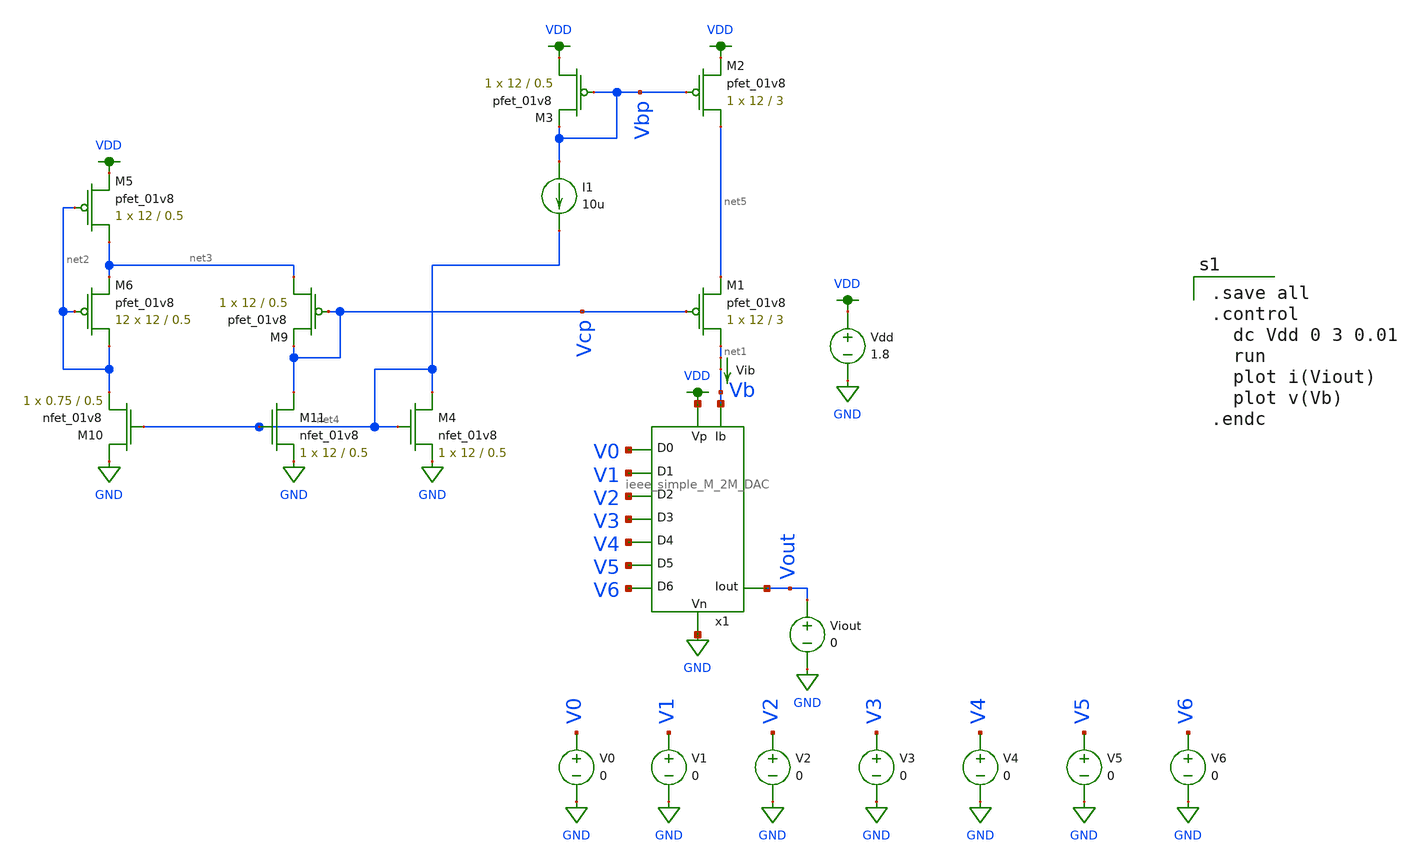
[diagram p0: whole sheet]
** sch_path: schematics/ieee DAC/characterization/top_voltage_sweep_with_cascode_and_vcn_generator.sch
**.subckt top_voltage_sweep_with_cascode_and_vcn_generator
Vdd VDD GND 1.8
V1 V1 GND 0
V2 V2 GND 0
V3 V3 GND 0
V4 V4 GND 0
V5 V5 GND 0
V6 V6 GND 0
V0 V0 GND 0
Viout Vout GND 0
Vib net1 Vb 0
.save i(vib)
x1 VDD Vout GND V1 V0 V2 V3 V4 V5 V6 Vb ieee_simple_M_2M_DAC
XM1 net1 Vcp net5 VDD sky130_fd_pr__pfet_01v8 L=3 W=12 nf=1 ad='int((nf+1)/2) * W/nf * 0.29' as='int((nf+2)/2) * W/nf * 0.29'
+ pd='2*int((nf+1)/2) * (W/nf + 0.29)' ps='2*int((nf+2)/2) * (W/nf + 0.29)' nrd='0.29 / W' nrs='0.29 / W'
+ sa=0 sb=0 sd=0 mult=1 m=1
XM5 net3 net2 VDD VDD sky130_fd_pr__pfet_01v8 L=0.5 W=12 nf=1 ad='int((nf+1)/2) * W/nf * 0.29' as='int((nf+2)/2) * W/nf * 0.29'
+ pd='2*int((nf+1)/2) * (W/nf + 0.29)' ps='2*int((nf+2)/2) * (W/nf + 0.29)' nrd='0.29 / W' nrs='0.29 / W'
+ sa=0 sb=0 sd=0 mult=1 m=1
XM6 net2 net2 net3 VDD sky130_fd_pr__pfet_01v8 L=0.5 W=12 nf=1 ad='int((nf+1)/2) * W/nf * 0.29' as='int((nf+2)/2) * W/nf * 0.29'
+ pd='2*int((nf+1)/2) * (W/nf + 0.29)' ps='2*int((nf+2)/2) * (W/nf + 0.29)' nrd='0.29 / W' nrs='0.29 / W'
+ sa=0 sb=0 sd=0 mult=12 m=12
XM9 net3 Vcp Vcp VDD sky130_fd_pr__pfet_01v8 L=0.5 W=12 nf=1 ad='int((nf+1)/2) * W/nf * 0.29' as='int((nf+2)/2) * W/nf * 0.29'
+ pd='2*int((nf+1)/2) * (W/nf + 0.29)' ps='2*int((nf+2)/2) * (W/nf + 0.29)' nrd='0.29 / W' nrs='0.29 / W'
+ sa=0 sb=0 sd=0 mult=1 m=1
XM10 GND net4 net2 GND sky130_fd_pr__nfet_01v8 L=0.5 W=0.75 nf=1 ad='int((nf+1)/2) * W/nf * 0.29' as='int((nf+2)/2) * W/nf * 0.29'
+ pd='2*int((nf+1)/2) * (W/nf + 0.29)' ps='2*int((nf+2)/2) * (W/nf + 0.29)' nrd='0.29 / W' nrs='0.29 / W'
+ sa=0 sb=0 sd=0 mult=1 m=1
XM11 Vcp net4 GND GND sky130_fd_pr__nfet_01v8 L=0.5 W=12 nf=1 ad='int((nf+1)/2) * W/nf * 0.29' as='int((nf+2)/2) * W/nf * 0.29'
+ pd='2*int((nf+1)/2) * (W/nf + 0.29)' ps='2*int((nf+2)/2) * (W/nf + 0.29)' nrd='0.29 / W' nrs='0.29 / W'
+ sa=0 sb=0 sd=0 mult=1 m=1
I1 Vbp net4 10u
XM2 net5 Vbp VDD VDD sky130_fd_pr__pfet_01v8 L=3 W=12 nf=1 ad='int((nf+1)/2) * W/nf * 0.29' as='int((nf+2)/2) * W/nf * 0.29'
+ pd='2*int((nf+1)/2) * (W/nf + 0.29)' ps='2*int((nf+2)/2) * (W/nf + 0.29)' nrd='0.29 / W' nrs='0.29 / W'
+ sa=0 sb=0 sd=0 mult=1 m=1
XM3 VDD Vbp Vbp VDD sky130_fd_pr__pfet_01v8 L=0.5 W=12 nf=1 ad='int((nf+1)/2) * W/nf * 0.29' as='int((nf+2)/2) * W/nf * 0.29'
+ pd='2*int((nf+1)/2) * (W/nf + 0.29)' ps='2*int((nf+2)/2) * (W/nf + 0.29)' nrd='0.29 / W' nrs='0.29 / W'
+ sa=0 sb=0 sd=0 mult=1 m=1
XM4 net4 net4 GND GND sky130_fd_pr__nfet_01v8 L=0.5 W=12 nf=1 ad='int((nf+1)/2) * W/nf * 0.29' as='int((nf+2)/2) * W/nf * 0.29'
+ pd='2*int((nf+1)/2) * (W/nf + 0.29)' ps='2*int((nf+2)/2) * (W/nf + 0.29)' nrd='0.29 / W' nrs='0.29 / W'
+ sa=0 sb=0 sd=0 mult=1 m=1
**** begin user architecture code

.option wnflag=1
.param MC_SWITCH=1.0
.lib ~/skywater/skywater-pdk/libraries/sky130_fd_pr_ngspice/latest/models/sky130.lib.spice tt


.save all
.control
  dc Vdd 0 3 0.01
  run
  plot i(Viout)
  plot v(Vb)
.endc

**** end user architecture code
**.ends

* expanding   symbol:  /home/madvlsi/dev/git/7-bit-D-A-converter-MP4-MADVLSI/schematics/ieee
*+ DAC/ieee_simple_M_2M_DAC.sym # of pins=11
** sym_path: mp4_submission/DAC/schematics/ieee_simple_M_2M_DAC.sym
** sch_path: mp4_submission/DAC/schematics/ieee_simple_M_2M_DAC.sch
.subckt ieee_simple_M_2M_DAC VDD Iout GND D1 D0 D2 D3 D4 D5 D6 Ibias
*.ipin Ibias
*.opin Iout
*.ipin D0
*.ipin D1
*.ipin D2
*.ipin D3
*.ipin D4
*.ipin D5
*.ipin D6
*.iopin VDD
*.iopin GND
x1 VDD GND net8 GND inverter
x2 VDD D0 net1 GND inverter
x3 VDD D1 net2 GND inverter
x4 VDD D2 net3 GND inverter
x5 VDD D3 net4 GND inverter
x6 VDD D4 net5 GND inverter
x7 VDD D5 net6 GND inverter
x8 VDD D6 net7 GND inverter
x9 Ibias net8 net1 net3 net4 net5 net6 D5 net2 D0 D1 D2 D3 D4 net7 D6 Iout GND ieee_DAC
.ends


* expanding   symbol:  /home/madvlsi/dev/git/7-bit-D-A-converter-MP4-MADVLSI/schematics/ieee
*+ DAC/inverter.sym # of pins=4
** sym_path: schematics/ieee DAC/inverter.sym
** sch_path: schematics/ieee DAC/inverter.sch
.subckt inverter VDD A Y GND
*.ipin A
*.iopin VDD
*.iopin GND
*.opin Y
XM1 Y A GND GND sky130_fd_pr__nfet_01v8 L=0.5 W=12 nf=1 ad='int((nf+1)/2) * W/nf * 0.29' as='int((nf+2)/2) * W/nf * 0.29'
+ pd='2*int((nf+1)/2) * (W/nf + 0.29)' ps='2*int((nf+2)/2) * (W/nf + 0.29)' nrd='0.29 / W' nrs='0.29 / W'
+ sa=0 sb=0 sd=0 mult=1 m=1
XM2 Y A VDD VDD sky130_fd_pr__pfet_01v8 L=0.5 W=12 nf=1 ad='int((nf+1)/2) * W/nf * 0.29' as='int((nf+2)/2) * W/nf * 0.29'
+ pd='2*int((nf+1)/2) * (W/nf + 0.29)' ps='2*int((nf+2)/2) * (W/nf + 0.29)' nrd='0.29 / W' nrs='0.29 / W'
+ sa=0 sb=0 sd=0 mult=1 m=1
.ends


* expanding   symbol:  /home/madvlsi/dev/git/7-bit-D-A-converter-MP4-MADVLSI/schematics/ieee
*+ DAC/ieee_DAC.sym # of pins=18
** sym_path: schematics/ieee DAC/ieee_DAC.sym
** sch_path: schematics/ieee DAC/ieee_DAC.sch
.subckt ieee_DAC Ibias Vg D0 D2 D3 D4 D5 D5b D1 D0b D1b D2b D3b D4b D6 D6b Iout Idump
*.ipin D0
*.ipin D1
*.ipin D2
*.ipin D3
*.ipin D4
*.ipin D5
*.ipin D6
*.ipin D0b
*.ipin D1b
*.ipin D2b
*.ipin D3b
*.ipin D4b
*.ipin D5b
*.ipin D6b
*.iopin Iout
*.iopin Idump
*.iopin Ibias
*.iopin Vg
XM1 Ibias Vg net12 GND sky130_fd_pr__nfet_01v8 L=0.5 W=12 nf=1 ad='int((nf+1)/2) * W/nf * 0.29' as='int((nf+2)/2) * W/nf * 0.29'
+ pd='2*int((nf+1)/2) * (W/nf + 0.29)' ps='2*int((nf+2)/2) * (W/nf + 0.29)' nrd='0.29 / W' nrs='0.29 / W'
+ sa=0 sb=0 sd=0 mult=1 m=1
XM4 Ibias Vg net1 GND sky130_fd_pr__nfet_01v8 L=0.5 W=12 nf=1 ad='int((nf+1)/2) * W/nf * 0.29' as='int((nf+2)/2) * W/nf * 0.29'
+ pd='2*int((nf+1)/2) * (W/nf + 0.29)' ps='2*int((nf+2)/2) * (W/nf + 0.29)' nrd='0.29 / W' nrs='0.29 / W'
+ sa=0 sb=0 sd=0 mult=1 m=1
XM5 net1 Vg net11 GND sky130_fd_pr__nfet_01v8 L=0.5 W=12 nf=1 ad='int((nf+1)/2) * W/nf * 0.29' as='int((nf+2)/2) * W/nf * 0.29'
+ pd='2*int((nf+1)/2) * (W/nf + 0.29)' ps='2*int((nf+2)/2) * (W/nf + 0.29)' nrd='0.29 / W' nrs='0.29 / W'
+ sa=0 sb=0 sd=0 mult=1 m=1
XM8 net1 Vg net2 GND sky130_fd_pr__nfet_01v8 L=0.5 W=12 nf=1 ad='int((nf+1)/2) * W/nf * 0.29' as='int((nf+2)/2) * W/nf * 0.29'
+ pd='2*int((nf+1)/2) * (W/nf + 0.29)' ps='2*int((nf+2)/2) * (W/nf + 0.29)' nrd='0.29 / W' nrs='0.29 / W'
+ sa=0 sb=0 sd=0 mult=1 m=1
XM9 net2 Vg net10 GND sky130_fd_pr__nfet_01v8 L=0.5 W=12 nf=1 ad='int((nf+1)/2) * W/nf * 0.29' as='int((nf+2)/2) * W/nf * 0.29'
+ pd='2*int((nf+1)/2) * (W/nf + 0.29)' ps='2*int((nf+2)/2) * (W/nf + 0.29)' nrd='0.29 / W' nrs='0.29 / W'
+ sa=0 sb=0 sd=0 mult=1 m=1
XM12 net2 Vg net3 GND sky130_fd_pr__nfet_01v8 L=0.5 W=12 nf=1 ad='int((nf+1)/2) * W/nf * 0.29' as='int((nf+2)/2) * W/nf * 0.29'
+ pd='2*int((nf+1)/2) * (W/nf + 0.29)' ps='2*int((nf+2)/2) * (W/nf + 0.29)' nrd='0.29 / W' nrs='0.29 / W'
+ sa=0 sb=0 sd=0 mult=1 m=1
XM13 net3 Vg net9 GND sky130_fd_pr__nfet_01v8 L=0.5 W=12 nf=1 ad='int((nf+1)/2) * W/nf * 0.29' as='int((nf+2)/2) * W/nf * 0.29'
+ pd='2*int((nf+1)/2) * (W/nf + 0.29)' ps='2*int((nf+2)/2) * (W/nf + 0.29)' nrd='0.29 / W' nrs='0.29 / W'
+ sa=0 sb=0 sd=0 mult=1 m=1
XM16 net3 Vg net4 GND sky130_fd_pr__nfet_01v8 L=0.5 W=12 nf=1 ad='int((nf+1)/2) * W/nf * 0.29' as='int((nf+2)/2) * W/nf * 0.29'
+ pd='2*int((nf+1)/2) * (W/nf + 0.29)' ps='2*int((nf+2)/2) * (W/nf + 0.29)' nrd='0.29 / W' nrs='0.29 / W'
+ sa=0 sb=0 sd=0 mult=1 m=1
XM17 net4 Vg net8 GND sky130_fd_pr__nfet_01v8 L=0.5 W=12 nf=1 ad='int((nf+1)/2) * W/nf * 0.29' as='int((nf+2)/2) * W/nf * 0.29'
+ pd='2*int((nf+1)/2) * (W/nf + 0.29)' ps='2*int((nf+2)/2) * (W/nf + 0.29)' nrd='0.29 / W' nrs='0.29 / W'
+ sa=0 sb=0 sd=0 mult=1 m=1
XM7 net4 Vg net5 GND sky130_fd_pr__nfet_01v8 L=0.5 W=12 nf=1 ad='int((nf+1)/2) * W/nf * 0.29' as='int((nf+2)/2) * W/nf * 0.29'
+ pd='2*int((nf+1)/2) * (W/nf + 0.29)' ps='2*int((nf+2)/2) * (W/nf + 0.29)' nrd='0.29 / W' nrs='0.29 / W'
+ sa=0 sb=0 sd=0 mult=1 m=1
XM10 net5 Vg net7 GND sky130_fd_pr__nfet_01v8 L=0.5 W=12 nf=1 ad='int((nf+1)/2) * W/nf * 0.29' as='int((nf+2)/2) * W/nf * 0.29'
+ pd='2*int((nf+1)/2) * (W/nf + 0.29)' ps='2*int((nf+2)/2) * (W/nf + 0.29)' nrd='0.29 / W' nrs='0.29 / W'
+ sa=0 sb=0 sd=0 mult=1 m=1
XM15 net5 Vg net6 GND sky130_fd_pr__nfet_01v8 L=0.5 W=12 nf=1 ad='int((nf+1)/2) * W/nf * 0.29' as='int((nf+2)/2) * W/nf * 0.29'
+ pd='2*int((nf+1)/2) * (W/nf + 0.29)' ps='2*int((nf+2)/2) * (W/nf + 0.29)' nrd='0.29 / W' nrs='0.29 / W'
+ sa=0 sb=0 sd=0 mult=1 m=1
XM18 net6 Vg net13 GND sky130_fd_pr__nfet_01v8 L=0.5 W=12 nf=1 ad='int((nf+1)/2) * W/nf * 0.29' as='int((nf+2)/2) * W/nf * 0.29'
+ pd='2*int((nf+1)/2) * (W/nf + 0.29)' ps='2*int((nf+2)/2) * (W/nf + 0.29)' nrd='0.29 / W' nrs='0.29 / W'
+ sa=0 sb=0 sd=0 mult=1 m=1
XM2 net7 D5 Iout GND sky130_fd_pr__nfet_01v8 L=0.5 W=12 nf=1 ad='int((nf+1)/2) * W/nf * 0.29' as='int((nf+2)/2) * W/nf * 0.29'
+ pd='2*int((nf+1)/2) * (W/nf + 0.29)' ps='2*int((nf+2)/2) * (W/nf + 0.29)' nrd='0.29 / W' nrs='0.29 / W'
+ sa=0 sb=0 sd=0 mult=1 m=1
XM3 Idump D5b net7 GND sky130_fd_pr__nfet_01v8 L=0.5 W=12 nf=1 ad='int((nf+1)/2) * W/nf * 0.29' as='int((nf+2)/2) * W/nf * 0.29'
+ pd='2*int((nf+1)/2) * (W/nf + 0.29)' ps='2*int((nf+2)/2) * (W/nf + 0.29)' nrd='0.29 / W' nrs='0.29 / W'
+ sa=0 sb=0 sd=0 mult=1 m=1
XM6 net8 D4 Iout GND sky130_fd_pr__nfet_01v8 L=0.5 W=12 nf=1 ad='int((nf+1)/2) * W/nf * 0.29' as='int((nf+2)/2) * W/nf * 0.29'
+ pd='2*int((nf+1)/2) * (W/nf + 0.29)' ps='2*int((nf+2)/2) * (W/nf + 0.29)' nrd='0.29 / W' nrs='0.29 / W'
+ sa=0 sb=0 sd=0 mult=1 m=1
XM11 Idump D4b net8 GND sky130_fd_pr__nfet_01v8 L=0.5 W=12 nf=1 ad='int((nf+1)/2) * W/nf * 0.29' as='int((nf+2)/2) * W/nf * 0.29'
+ pd='2*int((nf+1)/2) * (W/nf + 0.29)' ps='2*int((nf+2)/2) * (W/nf + 0.29)' nrd='0.29 / W' nrs='0.29 / W'
+ sa=0 sb=0 sd=0 mult=1 m=1
XM14 net9 D3 Iout GND sky130_fd_pr__nfet_01v8 L=0.5 W=12 nf=1 ad='int((nf+1)/2) * W/nf * 0.29' as='int((nf+2)/2) * W/nf * 0.29'
+ pd='2*int((nf+1)/2) * (W/nf + 0.29)' ps='2*int((nf+2)/2) * (W/nf + 0.29)' nrd='0.29 / W' nrs='0.29 / W'
+ sa=0 sb=0 sd=0 mult=1 m=1
XM19 Idump D3b net9 GND sky130_fd_pr__nfet_01v8 L=0.5 W=12 nf=1 ad='int((nf+1)/2) * W/nf * 0.29' as='int((nf+2)/2) * W/nf * 0.29'
+ pd='2*int((nf+1)/2) * (W/nf + 0.29)' ps='2*int((nf+2)/2) * (W/nf + 0.29)' nrd='0.29 / W' nrs='0.29 / W'
+ sa=0 sb=0 sd=0 mult=1 m=1
XM20 net10 D2 Iout GND sky130_fd_pr__nfet_01v8 L=0.5 W=12 nf=1 ad='int((nf+1)/2) * W/nf * 0.29' as='int((nf+2)/2) * W/nf * 0.29'
+ pd='2*int((nf+1)/2) * (W/nf + 0.29)' ps='2*int((nf+2)/2) * (W/nf + 0.29)' nrd='0.29 / W' nrs='0.29 / W'
+ sa=0 sb=0 sd=0 mult=1 m=1
XM21 Idump D2b net10 GND sky130_fd_pr__nfet_01v8 L=0.5 W=12 nf=1 ad='int((nf+1)/2) * W/nf * 0.29' as='int((nf+2)/2) * W/nf * 0.29'
+ pd='2*int((nf+1)/2) * (W/nf + 0.29)' ps='2*int((nf+2)/2) * (W/nf + 0.29)' nrd='0.29 / W' nrs='0.29 / W'
+ sa=0 sb=0 sd=0 mult=1 m=1
XM22 net11 D1 Iout GND sky130_fd_pr__nfet_01v8 L=0.5 W=12 nf=1 ad='int((nf+1)/2) * W/nf * 0.29' as='int((nf+2)/2) * W/nf * 0.29'
+ pd='2*int((nf+1)/2) * (W/nf + 0.29)' ps='2*int((nf+2)/2) * (W/nf + 0.29)' nrd='0.29 / W' nrs='0.29 / W'
+ sa=0 sb=0 sd=0 mult=1 m=1
XM23 Idump D1b net11 GND sky130_fd_pr__nfet_01v8 L=0.5 W=12 nf=1 ad='int((nf+1)/2) * W/nf * 0.29' as='int((nf+2)/2) * W/nf * 0.29'
+ pd='2*int((nf+1)/2) * (W/nf + 0.29)' ps='2*int((nf+2)/2) * (W/nf + 0.29)' nrd='0.29 / W' nrs='0.29 / W'
+ sa=0 sb=0 sd=0 mult=1 m=1
XM24 net12 D0 Iout GND sky130_fd_pr__nfet_01v8 L=0.5 W=12 nf=1 ad='int((nf+1)/2) * W/nf * 0.29' as='int((nf+2)/2) * W/nf * 0.29'
+ pd='2*int((nf+1)/2) * (W/nf + 0.29)' ps='2*int((nf+2)/2) * (W/nf + 0.29)' nrd='0.29 / W' nrs='0.29 / W'
+ sa=0 sb=0 sd=0 mult=1 m=1
XM25 Idump D0b net12 GND sky130_fd_pr__nfet_01v8 L=0.5 W=12 nf=1 ad='int((nf+1)/2) * W/nf * 0.29' as='int((nf+2)/2) * W/nf * 0.29'
+ pd='2*int((nf+1)/2) * (W/nf + 0.29)' ps='2*int((nf+2)/2) * (W/nf + 0.29)' nrd='0.29 / W' nrs='0.29 / W'
+ sa=0 sb=0 sd=0 mult=1 m=1
XM26 net13 D6 Iout GND sky130_fd_pr__nfet_01v8 L=0.5 W=12 nf=1 ad='int((nf+1)/2) * W/nf * 0.29' as='int((nf+2)/2) * W/nf * 0.29'
+ pd='2*int((nf+1)/2) * (W/nf + 0.29)' ps='2*int((nf+2)/2) * (W/nf + 0.29)' nrd='0.29 / W' nrs='0.29 / W'
+ sa=0 sb=0 sd=0 mult=1 m=1
XM27 Idump D6b net13 GND sky130_fd_pr__nfet_01v8 L=0.5 W=12 nf=1 ad='int((nf+1)/2) * W/nf * 0.29' as='int((nf+2)/2) * W/nf * 0.29'
+ pd='2*int((nf+1)/2) * (W/nf + 0.29)' ps='2*int((nf+2)/2) * (W/nf + 0.29)' nrd='0.29 / W' nrs='0.29 / W'
+ sa=0 sb=0 sd=0 mult=1 m=1
XM28 net6 Vg net14 GND sky130_fd_pr__nfet_01v8 L=0.5 W=12 nf=1 ad='int((nf+1)/2) * W/nf * 0.29' as='int((nf+2)/2) * W/nf * 0.29'
+ pd='2*int((nf+1)/2) * (W/nf + 0.29)' ps='2*int((nf+2)/2) * (W/nf + 0.29)' nrd='0.29 / W' nrs='0.29 / W'
+ sa=0 sb=0 sd=0 mult=1 m=1
XM29 net14 Vg Idump GND sky130_fd_pr__nfet_01v8 L=0.5 W=12 nf=1 ad='int((nf+1)/2) * W/nf * 0.29' as='int((nf+2)/2) * W/nf * 0.29'
+ pd='2*int((nf+1)/2) * (W/nf + 0.29)' ps='2*int((nf+2)/2) * (W/nf + 0.29)' nrd='0.29 / W' nrs='0.29 / W'
+ sa=0 sb=0 sd=0 mult=1 m=1
.ends

.GLOBAL VDD
.GLOBAL GND
.end
